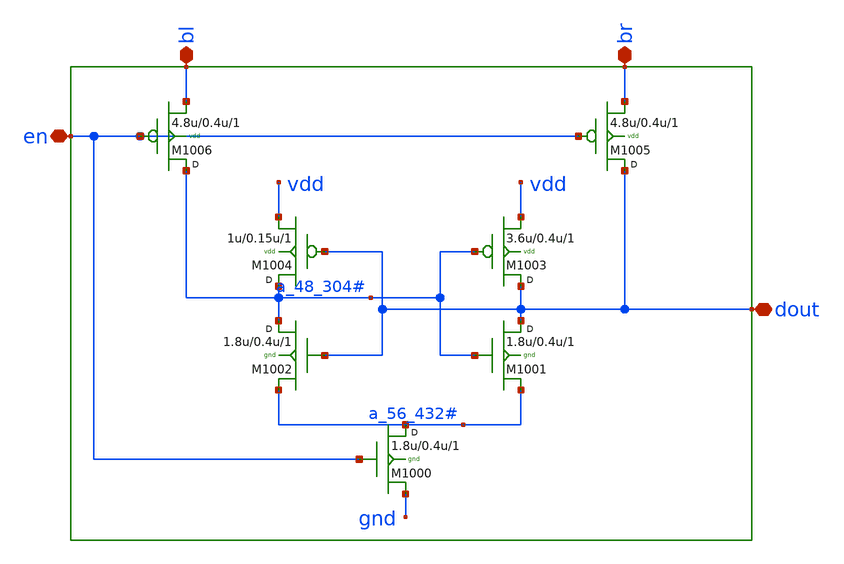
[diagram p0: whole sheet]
** sch_path: sram_2_64_scn4m/sense_amp.sch
**.subckt sense_amp bl br dout en
*.iopin bl
*.iopin br
*.iopin dout
*.iopin en
M1004 a_48_304# dout vdd vdd p w=1u l=0.15u m=1
M1003 dout a_48_304# vdd vdd p w=3.6u l=0.4u m=1
M1002 a_48_304# dout a_56_432# gnd n w=1.8u l=0.4u m=1
M1001 dout a_48_304# a_56_432# gnd n w=1.8u l=0.4u m=1
M1000 a_56_432# en gnd gnd n w=1.8u l=0.4u m=1
M1006 a_48_304# en bl vdd p w=4.8u l=0.4u m=1
M1005 dout en br vdd p w=4.8u l=0.4u m=1
**.ends
.end
